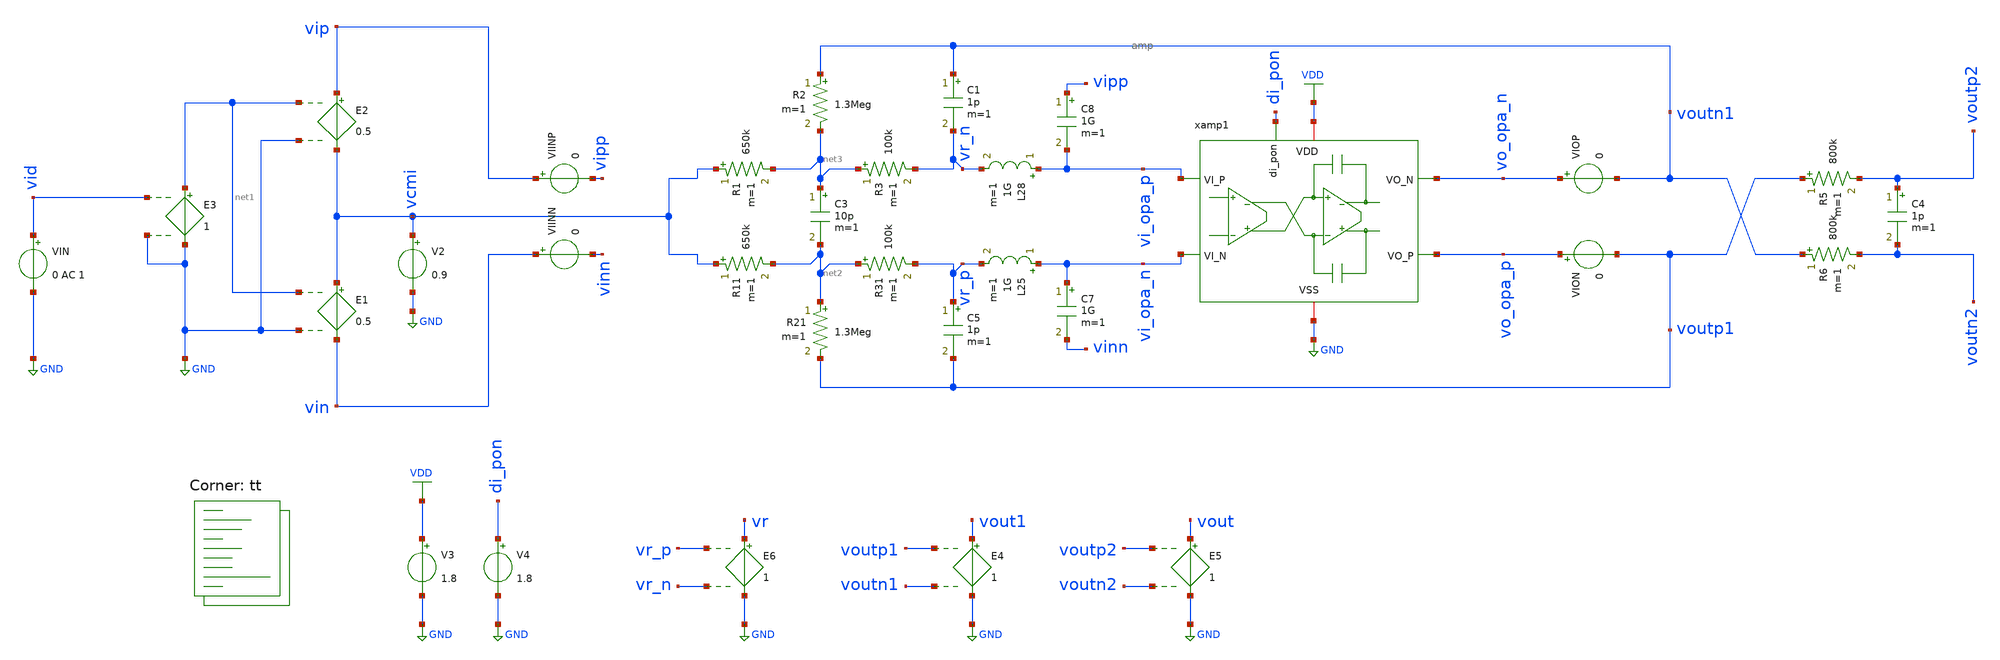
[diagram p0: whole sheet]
** sch_path: xschem/tb_filter_loopgain.sch
**.subckt tb_filter_loopgain
V2 vcmi GND 0.9
E1 vcmi vin net1 GND 0.5
E2 vip vcmi net1 GND 0.5
VIN vid GND 0 AC 1
E3 net1 GND vid GND 1
E4 vout1 GND voutp1 voutn1 1
VIINP vip vipp 0
VIINN vin vinn 0
R1 vcmi net3 650k m=1
R2 voutn1 net3 1.3Meg m=1
R3 net3 vr_n 100k m=1
C1 voutn1 vr_n 1p m=1
C3 net3 net2 10p m=1
R11 vcmi net2 650k m=1
R21 net2 voutp1 1.3Meg m=1
R31 net2 vr_p 100k m=1
C5 vr_p voutp1 1p m=1
E5 vout GND voutp2 voutn2 1
VIOP vo_opa_n voutn1 0
VION vo_opa_p voutp1 0
E6 vr GND vr_p vr_n 1
C7 vi_opa_n vinn 1G m=1
C8 vipp vi_opa_p 1G m=1
L25 vi_opa_n vr_p 1G m=1
L28 vi_opa_p vr_n 1G m=1
xamp1 VDD vi_opa_n vi_opa_p vo_opa_p di_pon vo_opa_n GND amp
V3 VDD GND 1.8
V4 di_pon GND 1.8
C4 voutp2 voutn2 1p m=1
R5 voutp1 voutp2 800k m=1
R6 voutn1 voutn2 800k m=1
**** begin user architecture code
.lib $::SKYWATER_MODELS/sky130.lib.spice tt


*.include /foss/designs/filter/ota_casc_3_dev_save.spice
.options savecurrents
.options method=gear reltol=.01
.options sparse
.control
save all

let f_sig = 100
let f_min = 10
let f_max = 100G
let f_stop = 5Meg
let tper_sig = 1/f_sig
let tfr_sig = tper_sig/2
let Adc = 10
let beta = 1/Adc
let v_step_o = 0.9
let v_step_i = v_step_o/Adc

let t_rf = 0.1u
let t_step = 50u
let t_delay = 0
let t_per = 2*t_step

let tstep = 0.1*t_rf
let tstop = 2*t_per
let tstart = t_delay

*alter @VIN[SIN] = [ 0 0.01 $&f_sig 0 0 0 ]
alter @VIN[DC] = 0.0


*set fndc = /foss/designs/frontend/frontend_dc.txt
*set fntran = /foss/designs/frontend/frontend_tran.txt
*set fnspec = /foss/designs/frontend/frontend_spec.txt
*set fnhd = /foss/designs/frontend/frontend_hd.txt
*set fnnoise = /foss/designs/frontend/frontend_noise.txt
set wr_singlescale
set wr_vecnames
option numdgt=3


** Main Simulations
	op
	ac dec 100 $&const.f_min $&const.f_max

	setplot ac1
	let A1 = v(vout1)/v(vid)
	let A2 = v(vout)/v(vid)
	let L = v(vr)/v(vid)
	let A = L/beta

	let L_re = real(L)
	let L_im = imag(L)

	let L_dB = vdb(L)
	let L_arg = 180/PI*cphase(L)
	let A_dB = vdb(A)
	let A_arg = 180/PI*cphase(A)

	let fdc = const.f_min+1

	meas ac fug find frequency when L_dB=0
	meas ac pm find L_arg when frequency=fug

	let pm = 180-abs(pm)

	print pm

	let err_gain = 1-10^(Adc/20)/10
	let Adc_ol_min = (1-err_gain)/err_gain

	print err_gain
	print Adc_ol_min

	plot L_dB L_arg A_dB A_arg title 'Bode Plot of Loop Gain' ylabel 'Magnitude (dB) / Phase (Deg)'
	plot L_im vs L_re retraceplot title 'Nyquist Plot of Loop Gain' ylabel 'Imaginary Part' xlabel 'Real Part'


alter @VIN[DC] = 0
op

remzerovec
write tb_filter_loopgain.raw
.endc

**** end user architecture code
**.ends

* expanding   symbol:  /foss/designs/xschem/amp.sym # of pins=7
** sym_path: xschem/amp.sym
** sch_path: xschem/amp.sch
.subckt amp VDD VI_N VI_P VO_P di_pon VO_N VSS
*.iopin VSS
*.iopin VDD
*.ipin VI_P
*.ipin di_pon
*.ipin VI_N
*.opin VO_N
*.opin VO_P
XMP1 vbp vbp VDD VDD sky130_fd_pr__pfet_01v8 L=0.25 W='5 * 5 ' nf=5 ad='int((nf+1)/2) * W / nf * 0.29'
+ as='int((nf+2)/2) * W / nf * 0.29' pd='2*int((nf+1)/2) * (W / nf + 0.29)' ps='2*int((nf+2)/2) * (W / nf + 0.29)'
+ nrd='0.29 / W ' nrs='0.29 / W ' sa=0 sb=0 sd=0 mult=1 m=1
XMPSW3 vbp pon VDD VDD sky130_fd_pr__pfet_01v8 L=0.15 W='5 * 5 ' nf=5 ad='int((nf+1)/2) * W / nf * 0.29'
+ as='int((nf+2)/2) * W / nf * 0.29' pd='2*int((nf+1)/2) * (W / nf + 0.29)' ps='2*int((nf+2)/2) * (W / nf + 0.29)'
+ nrd='0.29 / W ' nrs='0.29 / W ' sa=0 sb=0 sd=0 mult=1 m=1
XMNSW1 pon_b di_pon VSS VSS sky130_fd_pr__nfet_01v8 L=0.15 W='3 * 1 ' nf=1 ad='int((nf+1)/2) * W / nf * 0.29'
+ as='int((nf+2)/2) * W / nf * 0.29' pd='2*int((nf+1)/2) * (W / nf + 0.29)' ps='2*int((nf+2)/2) * (W / nf + 0.29)'
+ nrd='0.29 / W ' nrs='0.29 / W ' sa=0 sb=0 sd=0 mult=1 m=1
XMPSW1 pon_b di_pon VDD VDD sky130_fd_pr__pfet_01v8 L=0.15 W='5 * 1 ' nf=1 ad='int((nf+1)/2) * W / nf * 0.29'
+ as='int((nf+2)/2) * W / nf * 0.29' pd='2*int((nf+1)/2) * (W / nf + 0.29)' ps='2*int((nf+2)/2) * (W / nf + 0.29)'
+ nrd='0.29 / W ' nrs='0.29 / W ' sa=0 sb=0 sd=0 mult=1 m=1
XMNSW2 pon pon_b VSS VSS sky130_fd_pr__nfet_01v8 L=0.15 W='3 * 3 ' nf=3 ad='int((nf+1)/2) * W / nf * 0.29'
+ as='int((nf+2)/2) * W / nf * 0.29' pd='2*int((nf+1)/2) * (W / nf + 0.29)' ps='2*int((nf+2)/2) * (W / nf + 0.29)'
+ nrd='0.29 / W ' nrs='0.29 / W ' sa=0 sb=0 sd=0 mult=1 m=1
XMPSW2 pon pon_b VDD VDD sky130_fd_pr__pfet_01v8 L=0.15 W='5 * 3 ' nf=3 ad='int((nf+1)/2) * W / nf * 0.29'
+ as='int((nf+2)/2) * W / nf * 0.29' pd='2*int((nf+1)/2) * (W / nf + 0.29)' ps='2*int((nf+2)/2) * (W / nf + 0.29)'
+ nrd='0.29 / W ' nrs='0.29 / W ' sa=0 sb=0 sd=0 mult=1 m=1
XMP2 viref1 vbp VDD VDD sky130_fd_pr__pfet_01v8 L=0.25 W='5 * 50 ' nf=50 ad='int((nf+1)/2) * W / nf * 0.29'
+ as='int((nf+2)/2) * W / nf * 0.29' pd='2*int((nf+1)/2) * (W / nf + 0.29)' ps='2*int((nf+2)/2) * (W / nf + 0.29)'
+ nrd='0.29 / W ' nrs='0.29 / W ' sa=0 sb=0 sd=0 mult=1 m=1
XMP3 vfb2 vbp VDD VDD sky130_fd_pr__pfet_01v8 L=0.25 W='5 * 5 ' nf=5 ad='int((nf+1)/2) * W / nf * 0.29'
+ as='int((nf+2)/2) * W / nf * 0.29' pd='2*int((nf+1)/2) * (W / nf + 0.29)' ps='2*int((nf+2)/2) * (W / nf + 0.29)'
+ nrd='0.29 / W ' nrs='0.29 / W ' sa=0 sb=0 sd=0 mult=1 m=1
XC6 VDD vbp sky130_fd_pr__cap_mim_m3_1 W=5 L=5 MF=5 m=5
XMP4 voutn1 VI_P viref1 viref1 sky130_fd_pr__pfet_01v8 L=0.15 W='5 * 20 ' nf=20 ad='int((nf+1)/2) * W / nf * 0.29'
+ as='int((nf+2)/2) * W / nf * 0.29' pd='2*int((nf+1)/2) * (W / nf + 0.29)' ps='2*int((nf+2)/2) * (W / nf + 0.29)'
+ nrd='0.29 / W ' nrs='0.29 / W ' sa=0 sb=0 sd=0 mult=1 m=1
XMP5 voutp1 VI_N viref1 viref1 sky130_fd_pr__pfet_01v8 L=0.15 W='5 * 20 ' nf=20 ad='int((nf+1)/2) * W / nf * 0.29'
+ as='int((nf+2)/2) * W / nf * 0.29' pd='2*int((nf+1)/2) * (W / nf + 0.29)' ps='2*int((nf+2)/2) * (W / nf + 0.29)'
+ nrd='0.29 / W ' nrs='0.29 / W ' sa=0 sb=0 sd=0 mult=1 m=1
XMN1 voutn1 vfb1 VSS VSS sky130_fd_pr__nfet_01v8 L=0.5 W='3 * 1 ' nf=1 ad='int((nf+1)/2) * W / nf * 0.29'
+ as='int((nf+2)/2) * W / nf * 0.29' pd='2*int((nf+1)/2) * (W / nf + 0.29)' ps='2*int((nf+2)/2) * (W / nf + 0.29)'
+ nrd='0.29 / W ' nrs='0.29 / W ' sa=0 sb=0 sd=0 mult=1 m=1
XMN2 voutp1 vfb1 VSS VSS sky130_fd_pr__nfet_01v8 L=0.5 W='3 * 1 ' nf=1 ad='int((nf+1)/2) * W / nf * 0.29'
+ as='int((nf+2)/2) * W / nf * 0.29' pd='2*int((nf+1)/2) * (W / nf + 0.29)' ps='2*int((nf+2)/2) * (W / nf + 0.29)'
+ nrd='0.29 / W ' nrs='0.29 / W ' sa=0 sb=0 sd=0 mult=1 m=1
R1 voutn1 vfb1 40k m=1
R3 vfb1 voutp1 40k m=1
XMN3 VO_P voutn1 net1 VSS sky130_fd_pr__nfet_01v8 L=0.5 W='3 * 1 ' nf=1 ad='int((nf+1)/2) * W / nf * 0.29'
+ as='int((nf+2)/2) * W / nf * 0.29' pd='2*int((nf+1)/2) * (W / nf + 0.29)' ps='2*int((nf+2)/2) * (W / nf + 0.29)'
+ nrd='0.29 / W ' nrs='0.29 / W ' sa=0 sb=0 sd=0 mult=1 m=1
XMN4 VO_N voutp1 VSS VSS sky130_fd_pr__nfet_01v8 L=0.5 W='3 * 1 ' nf=1 ad='int((nf+1)/2) * W / nf * 0.29'
+ as='int((nf+2)/2) * W / nf * 0.29' pd='2*int((nf+1)/2) * (W / nf + 0.29)' ps='2*int((nf+2)/2) * (W / nf + 0.29)'
+ nrd='0.29 / W ' nrs='0.29 / W ' sa=0 sb=0 sd=0 mult=1 m=1
XMP6 VO_P vfb2 VDD VDD sky130_fd_pr__pfet_01v8 L=0.25 W='5 * 10 ' nf=10 ad='int((nf+1)/2) * W / nf * 0.29'
+ as='int((nf+2)/2) * W / nf * 0.29' pd='2*int((nf+1)/2) * (W / nf + 0.29)' ps='2*int((nf+2)/2) * (W / nf + 0.29)'
+ nrd='0.29 / W ' nrs='0.29 / W ' sa=0 sb=0 sd=0 mult=1 m=1
XMP7 VO_N vfb2 VDD VDD sky130_fd_pr__pfet_01v8 L=0.25 W='5 * 10 ' nf=10 ad='int((nf+1)/2) * W / nf * 0.29'
+ as='int((nf+2)/2) * W / nf * 0.29' pd='2*int((nf+1)/2) * (W / nf + 0.29)' ps='2*int((nf+2)/2) * (W / nf + 0.29)'
+ nrd='0.29 / W ' nrs='0.29 / W ' sa=0 sb=0 sd=0 mult=1 m=1
XC1 voutn1 vfb1 sky130_fd_pr__cap_mim_m3_1 W=5 L=5 MF=5 m=5
XC2 vfb1 voutp1 sky130_fd_pr__cap_mim_m3_1 W=5 L=5 MF=5 m=5
I0 vbp VSS 10u
R2 VO_P vfb2 40k m=1
R4 vfb2 VO_N 40k m=1
XC3 VO_P vfb2 sky130_fd_pr__cap_mim_m3_1 W=5 L=5 MF=5 m=5
XC4 vfb2 VO_N sky130_fd_pr__cap_mim_m3_1 W=5 L=5 MF=5 m=5
.ends

.GLOBAL GND
.GLOBAL VDD
.end
